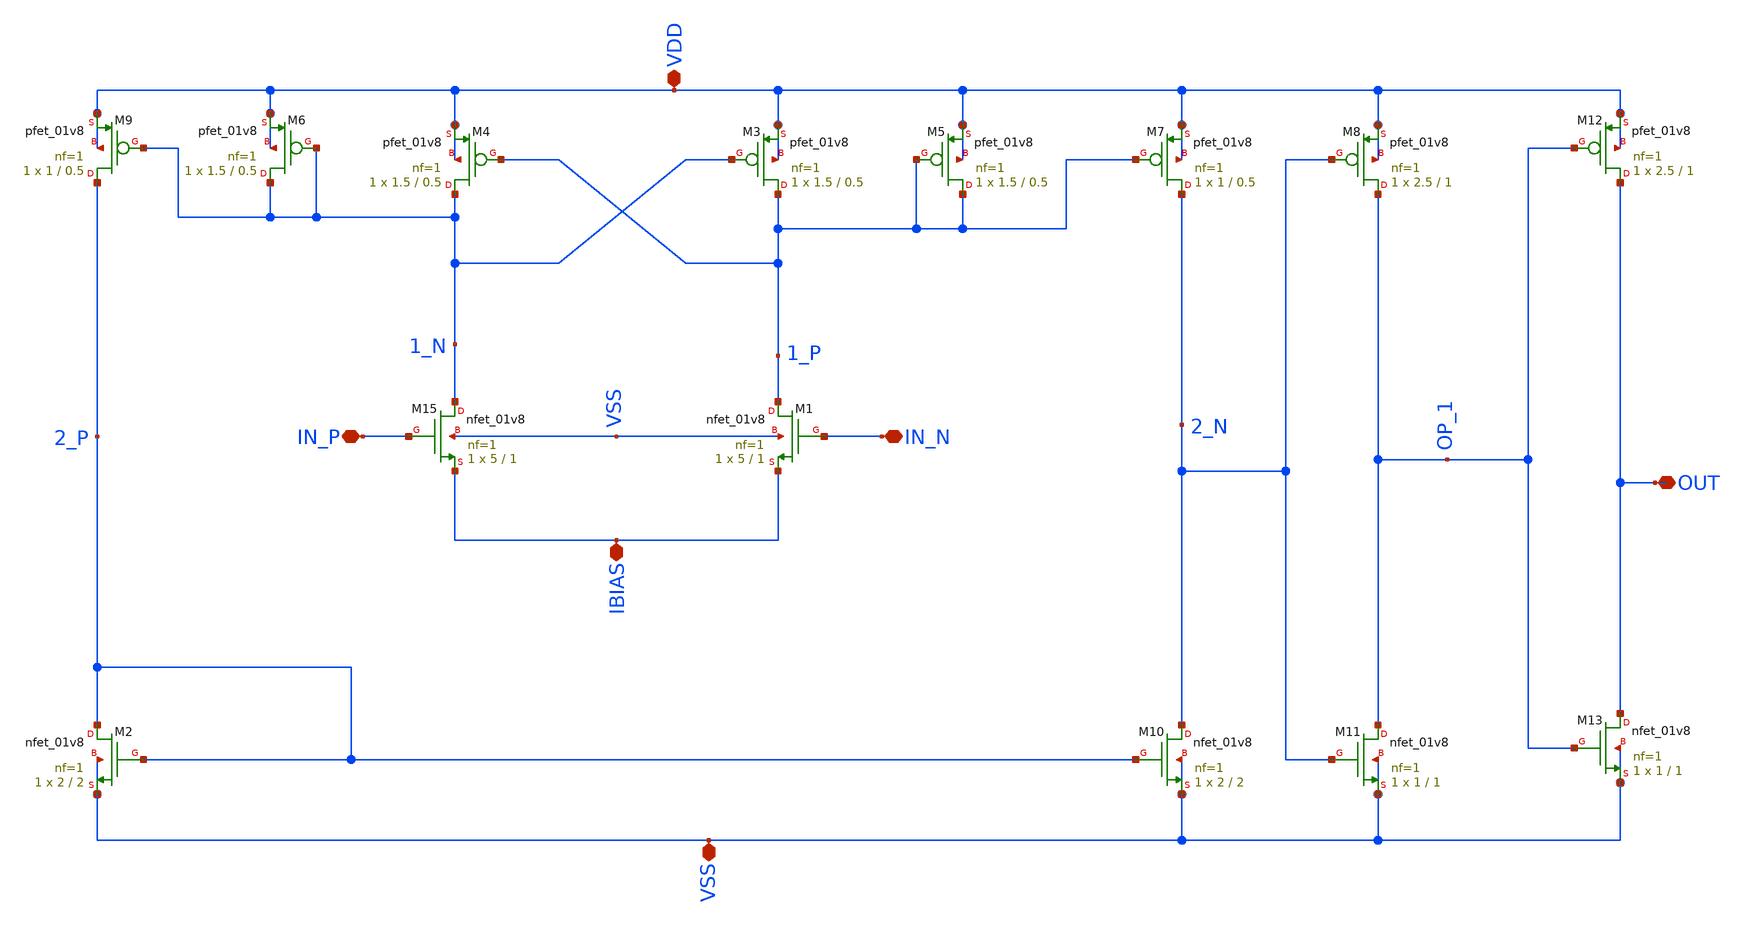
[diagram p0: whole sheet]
** sch_path: xschem/DC_DC_Converter_xschem/OTHERS/DC_DC_Converter_JV11/Comparator/Comparator.sch
**.subckt Comparator VDD VSS IN_P IN_N OUT IBIAS
*.iopin VDD
*.iopin VSS
*.iopin IN_P
*.iopin IN_N
*.iopin OUT
*.iopin IBIAS
XM15 1_N IN_P IBIAS VSS sky130_fd_pr__nfet_01v8 L=1 W=5 nf=1 ad='int((nf+1)/2) * W/nf * 0.29' as='int((nf+2)/2) * W/nf * 0.29'
+ pd='2*int((nf+1)/2) * (W/nf + 0.29)' ps='2*int((nf+2)/2) * (W/nf + 0.29)' nrd='0.29 / W' nrs='0.29 / W'
+ sa=0 sb=0 sd=0 mult=1 m=1
XM1 1_P IN_N IBIAS VSS sky130_fd_pr__nfet_01v8 L=1 W=5 nf=1 ad='int((nf+1)/2) * W/nf * 0.29' as='int((nf+2)/2) * W/nf * 0.29'
+ pd='2*int((nf+1)/2) * (W/nf + 0.29)' ps='2*int((nf+2)/2) * (W/nf + 0.29)' nrd='0.29 / W' nrs='0.29 / W'
+ sa=0 sb=0 sd=0 mult=1 m=1
XM2 2_P 2_P VSS VSS sky130_fd_pr__nfet_01v8 L=2 W=2 nf=1 ad='int((nf+1)/2) * W/nf * 0.29' as='int((nf+2)/2) * W/nf * 0.29'
+ pd='2*int((nf+1)/2) * (W/nf + 0.29)' ps='2*int((nf+2)/2) * (W/nf + 0.29)' nrd='0.29 / W' nrs='0.29 / W'
+ sa=0 sb=0 sd=0 mult=1 m=1
XM10 2_N 2_P VSS VSS sky130_fd_pr__nfet_01v8 L=2 W=2 nf=1 ad='int((nf+1)/2) * W/nf * 0.29' as='int((nf+2)/2) * W/nf * 0.29'
+ pd='2*int((nf+1)/2) * (W/nf + 0.29)' ps='2*int((nf+2)/2) * (W/nf + 0.29)' nrd='0.29 / W' nrs='0.29 / W'
+ sa=0 sb=0 sd=0 mult=1 m=1
XM11 OP_1 2_N VSS VSS sky130_fd_pr__nfet_01v8 L=1 W=1 nf=1 ad='int((nf+1)/2) * W/nf * 0.29' as='int((nf+2)/2) * W/nf * 0.29'
+ pd='2*int((nf+1)/2) * (W/nf + 0.29)' ps='2*int((nf+2)/2) * (W/nf + 0.29)' nrd='0.29 / W' nrs='0.29 / W'
+ sa=0 sb=0 sd=0 mult=1 m=1
XM13 OUT OP_1 VSS VSS sky130_fd_pr__nfet_01v8 L=1 W=1 nf=1 ad='int((nf+1)/2) * W/nf * 0.29' as='int((nf+2)/2) * W/nf * 0.29'
+ pd='2*int((nf+1)/2) * (W/nf + 0.29)' ps='2*int((nf+2)/2) * (W/nf + 0.29)' nrd='0.29 / W' nrs='0.29 / W'
+ sa=0 sb=0 sd=0 mult=1 m=1
XM9 2_P 1_N VDD VDD sky130_fd_pr__pfet_01v8 L=0.5 W=1 nf=1 ad='int((nf+1)/2) * W/nf * 0.29' as='int((nf+2)/2) * W/nf * 0.29'
+ pd='2*int((nf+1)/2) * (W/nf + 0.29)' ps='2*int((nf+2)/2) * (W/nf + 0.29)' nrd='0.29 / W' nrs='0.29 / W'
+ sa=0 sb=0 sd=0 mult=1 m=1
XM6 1_N 1_N VDD VDD sky130_fd_pr__pfet_01v8 L=0.5 W=1.5 nf=1 ad='int((nf+1)/2) * W/nf * 0.29' as='int((nf+2)/2) * W/nf * 0.29'
+ pd='2*int((nf+1)/2) * (W/nf + 0.29)' ps='2*int((nf+2)/2) * (W/nf + 0.29)' nrd='0.29 / W' nrs='0.29 / W'
+ sa=0 sb=0 sd=0 mult=1 m=1
XM4 1_N 1_P VDD VDD sky130_fd_pr__pfet_01v8 L=0.5 W=1.5 nf=1 ad='int((nf+1)/2) * W/nf * 0.29' as='int((nf+2)/2) * W/nf * 0.29'
+ pd='2*int((nf+1)/2) * (W/nf + 0.29)' ps='2*int((nf+2)/2) * (W/nf + 0.29)' nrd='0.29 / W' nrs='0.29 / W'
+ sa=0 sb=0 sd=0 mult=1 m=1
XM3 1_P 1_N VDD VDD sky130_fd_pr__pfet_01v8 L=0.5 W=1.5 nf=1 ad='int((nf+1)/2) * W/nf * 0.29' as='int((nf+2)/2) * W/nf * 0.29'
+ pd='2*int((nf+1)/2) * (W/nf + 0.29)' ps='2*int((nf+2)/2) * (W/nf + 0.29)' nrd='0.29 / W' nrs='0.29 / W'
+ sa=0 sb=0 sd=0 mult=1 m=1
XM5 1_P 1_P VDD VDD sky130_fd_pr__pfet_01v8 L=0.5 W=1.5 nf=1 ad='int((nf+1)/2) * W/nf * 0.29' as='int((nf+2)/2) * W/nf * 0.29'
+ pd='2*int((nf+1)/2) * (W/nf + 0.29)' ps='2*int((nf+2)/2) * (W/nf + 0.29)' nrd='0.29 / W' nrs='0.29 / W'
+ sa=0 sb=0 sd=0 mult=1 m=1
XM7 2_N 1_P VDD VDD sky130_fd_pr__pfet_01v8 L=0.5 W=1 nf=1 ad='int((nf+1)/2) * W/nf * 0.29' as='int((nf+2)/2) * W/nf * 0.29'
+ pd='2*int((nf+1)/2) * (W/nf + 0.29)' ps='2*int((nf+2)/2) * (W/nf + 0.29)' nrd='0.29 / W' nrs='0.29 / W'
+ sa=0 sb=0 sd=0 mult=1 m=1
XM8 OP_1 2_N VDD VDD sky130_fd_pr__pfet_01v8 L=1 W=2.5 nf=1 ad='int((nf+1)/2) * W/nf * 0.29' as='int((nf+2)/2) * W/nf * 0.29'
+ pd='2*int((nf+1)/2) * (W/nf + 0.29)' ps='2*int((nf+2)/2) * (W/nf + 0.29)' nrd='0.29 / W' nrs='0.29 / W'
+ sa=0 sb=0 sd=0 mult=1 m=1
XM12 OUT OP_1 VDD VDD sky130_fd_pr__pfet_01v8 L=1 W=2.5 nf=1 ad='int((nf+1)/2) * W/nf * 0.29' as='int((nf+2)/2) * W/nf * 0.29'
+ pd='2*int((nf+1)/2) * (W/nf + 0.29)' ps='2*int((nf+2)/2) * (W/nf + 0.29)' nrd='0.29 / W' nrs='0.29 / W'
+ sa=0 sb=0 sd=0 mult=1 m=1
**.ends
.end
